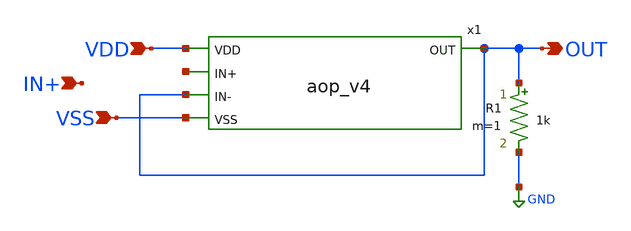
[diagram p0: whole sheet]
** sch_path: design/JNW_GR01_SKY130A/test_aop.sch
**.subckt test_aop VDD VSS IN+ OUT
*.ipin VDD
*.ipin VSS
*.ipin IN+
*.opin OUT
x1 OUT VDD net1 OUT VSS aop_v4
R1 OUT GND 1k m=1
**.ends
.GLOBAL GND
.end
